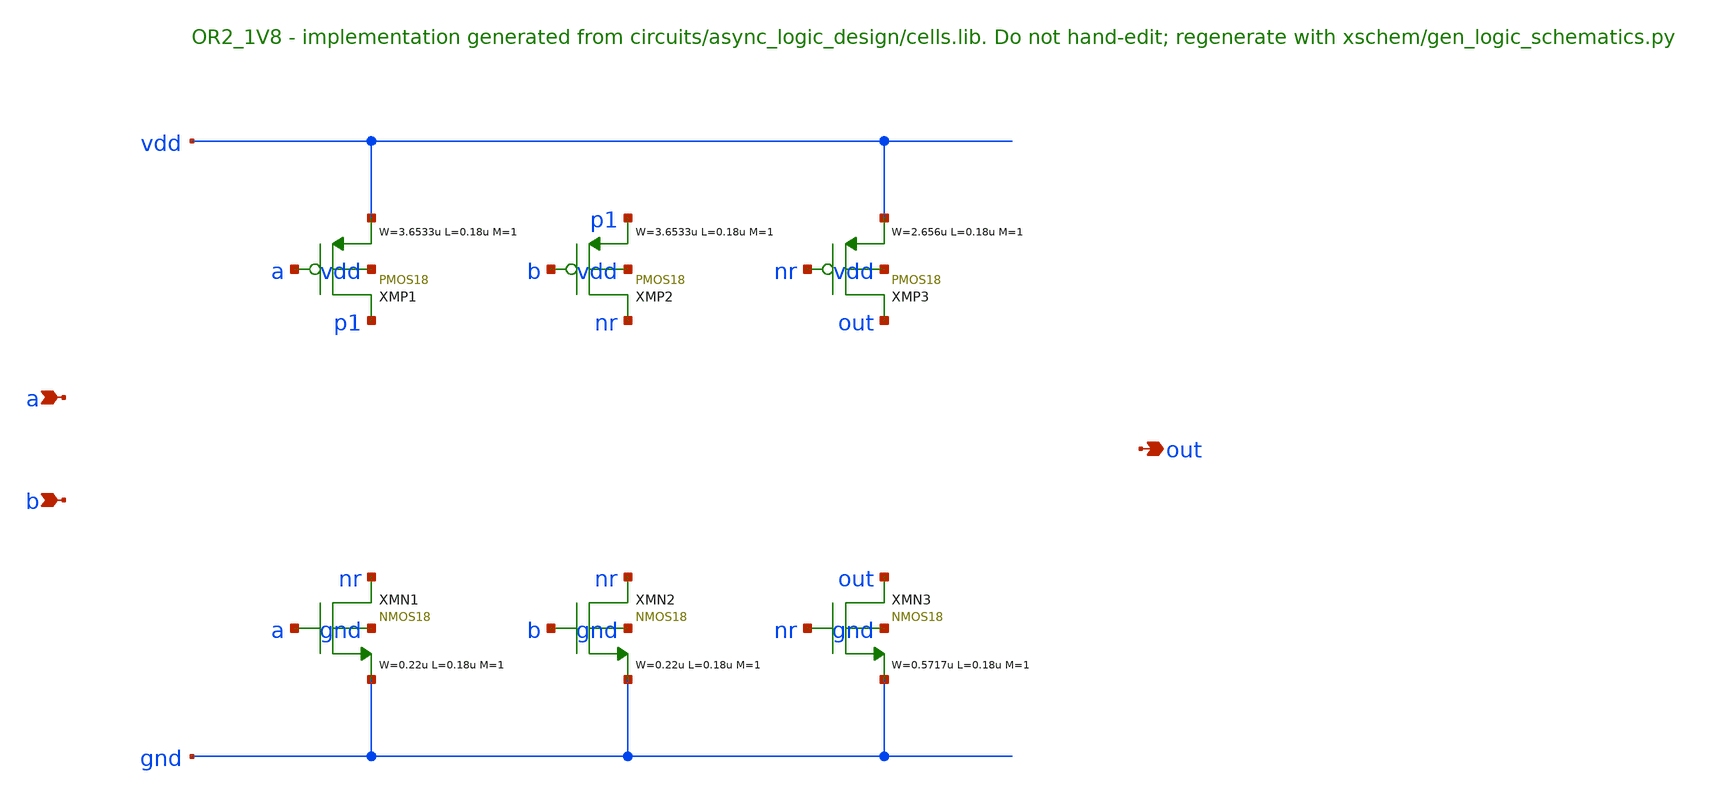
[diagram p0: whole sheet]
** sch_path: xschem/logic/OR2_1V8.sch
**.subckt OR2_1V8 a b out
*.ipin a
*.ipin b
*.opin out
XMP1 p1 a vdd vdd PMOS18 W=3.6533u L=0.18u M=1 MM_SIGMA=0
XMP2 nr b p1 vdd PMOS18 W=3.6533u L=0.18u M=1 MM_SIGMA=0
XMP3 out nr vdd vdd PMOS18 W=2.656u L=0.18u M=1 MM_SIGMA=0
XMN1 nr a gnd gnd NMOS18 W=0.22u L=0.18u M=1 MM_SIGMA=0
XMN2 nr b gnd gnd NMOS18 W=0.22u L=0.18u M=1 MM_SIGMA=0
XMN3 out nr gnd gnd NMOS18 W=0.5717u L=0.18u M=1 MM_SIGMA=0
**.ends
.end
